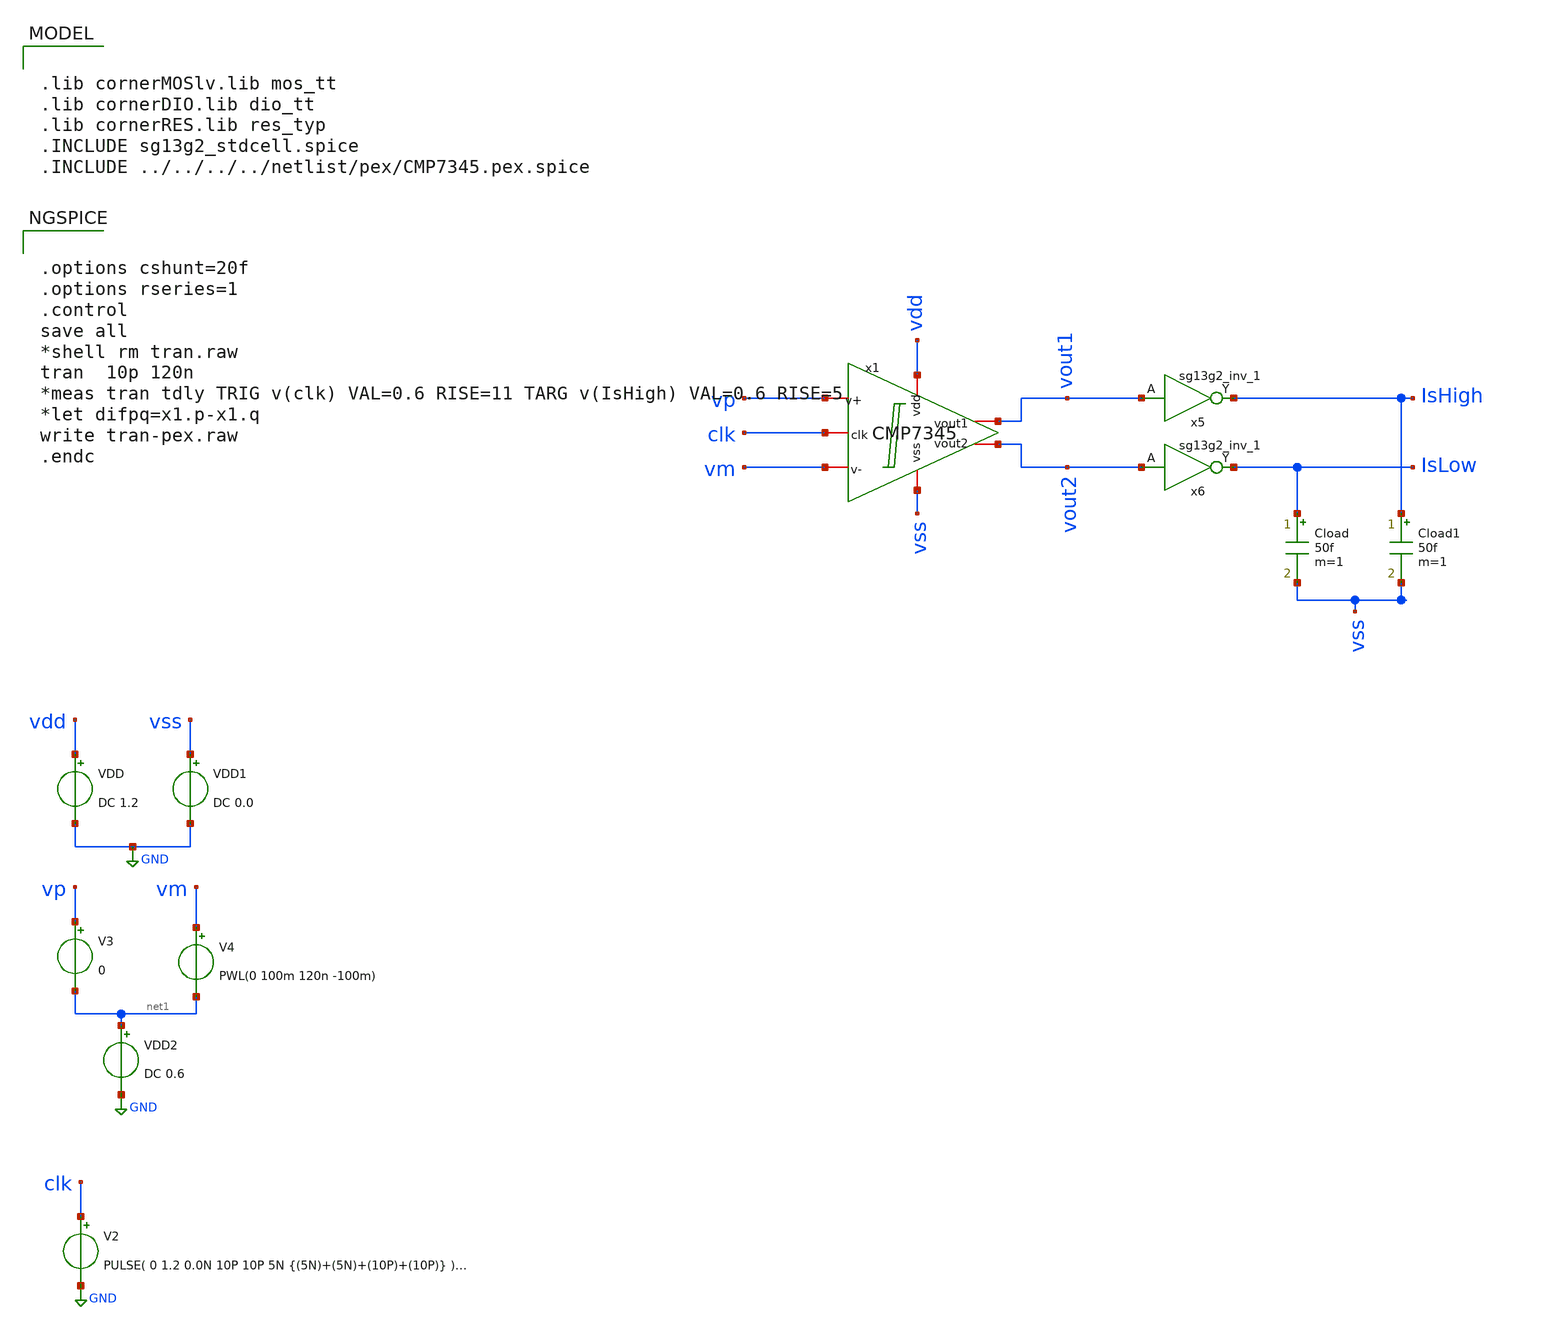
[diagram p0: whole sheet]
** sch_path: CMP7345-main/testbenches/tran/xschem/CMP7345_pex_tb.sch
**.subckt CMP7345_pex_tb
VDD vdd GND DC 1.2
Cload IsLow vss 50f m=1
VDD1 vss GND DC 0.0
Cload1 IsHigh vss 50f m=1
V2 clk GND PULSE( 0 1.2 0.0N 10P 10P 5N {(5N)+(5N)+(10P)+(10P)} ) AC 0
V3 vp net1 0
VDD2 net1 GND DC 0.6
x5 IsHigh vout1 VDD VSS sg13g2_inv_1
x6 IsLow vout2 VDD VSS sg13g2_inv_1
V4 vm net1 PWL(0 100m 120n -100m)
x1 vdd vout1 vout2 vp vm clk vss CMP7345
**** begin user architecture code

.lib cornerMOSlv.lib mos_tt
.lib cornerDIO.lib dio_tt
.lib cornerRES.lib res_typ
.INCLUDE sg13g2_stdcell.spice
.INCLUDE ../../../../netlist/pex/CMP7345.pex.spice



.options cshunt=20f
.options rseries=1
.control
save all
*shell rm tran.raw
tran  10p 120n
*meas tran tdly TRIG v(clk) VAL=0.6 RISE=11 TARG v(IsHigh) VAL=0.6 RISE=5
*let difpq=x1.p-x1.q
write tran-pex.raw
.endc


**** end user architecture code
**.ends

* expanding   symbol:  sg13g2_stdcells/sg13g2_inv_1.sym # of pins=2
** sym_path: sg13g2_stdcells/sg13g2_inv_1.sym
** sch_path: sg13g2_stdcells/sg13g2_inv_1.sch
.subckt sg13g2_inv_1 Y A VDD VSS
*.opin Y
*.ipin A
*.iopin VDD
*.iopin VSS
XM1 Y A VSS VSS sg13_lv_nmos w=740.00n l=130.00n ng=1 m=1 mm_ok=1
XM2 Y A VDD VDD sg13_lv_pmos w=1.12u l=130.00n ng=1 m=1 mm_ok=1
.ends

.GLOBAL GND
.end
